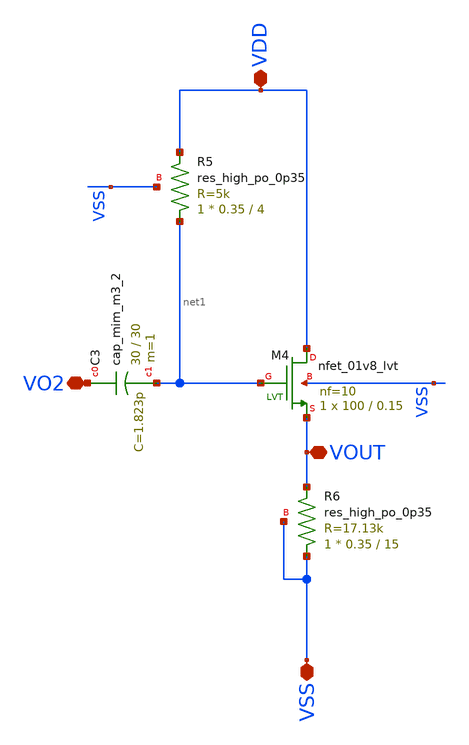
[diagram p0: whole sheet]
** sch_path: xschem/xschem4_sic_oct_20/partition5.sch
**.subckt partition5 VOUT VDD VSS VO2
*.iopin VOUT
*.iopin VDD
*.iopin VSS
*.iopin VO2
XM4 VDD net1 VOUT VSS sky130_fd_pr__nfet_01v8_lvt L=0.15 W=100 nf=10 ad='int((nf+1)/2) * W/nf * 0.29'
+ as='int((nf+2)/2) * W/nf * 0.29' pd='2*int((nf+1)/2) * (W/nf + 0.29)' ps='2*int((nf+2)/2) * (W/nf + 0.29)'
+ nrd='0.29 / W' nrs='0.29 / W' sa=0 sb=0 sd=0 mult=1 m=1
XR5 net1 VDD VSS sky130_fd_pr__res_high_po_0p35 L=4 mult=1 m=1
XR6 VSS VOUT VSS sky130_fd_pr__res_high_po_0p35 L=15 mult=1 m=1
XC3 VO2 net1 sky130_fd_pr__cap_mim_m3_2 W=30 L=30 MF=1 m=1
**.ends
.end
